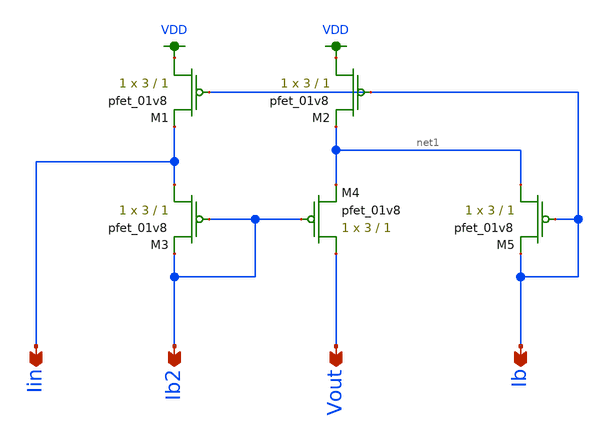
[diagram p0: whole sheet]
** sch_path: schematic/low-voltage_super-wilson.sch
**.subckt low-voltage_super-wilson Vout Ib Ib2 Iin
*.opin Vout
*.opin Ib
*.opin Ib2
*.opin Iin
XM1 VDD Ib Iin VDD sky130_fd_pr__pfet_01v8 L=1 W=3 nf=1 ad='int((nf+1)/2) * W/nf * 0.29' as='int((nf+2)/2) * W/nf * 0.29'
+ pd='2*int((nf+1)/2) * (W/nf + 0.29)' ps='2*int((nf+2)/2) * (W/nf + 0.29)' nrd='0.29 / W' nrs='0.29 / W'
+ sa=0 sb=0 sd=0 mult=1 m=1
XM2 VDD Ib net1 VDD sky130_fd_pr__pfet_01v8 L=1 W=3 nf=1 ad='int((nf+1)/2) * W/nf * 0.29' as='int((nf+2)/2) * W/nf * 0.29'
+ pd='2*int((nf+1)/2) * (W/nf + 0.29)' ps='2*int((nf+2)/2) * (W/nf + 0.29)' nrd='0.29 / W' nrs='0.29 / W'
+ sa=0 sb=0 sd=0 mult=1 m=1
XM3 Iin Ib2 Ib2 VDD sky130_fd_pr__pfet_01v8 L=1 W=3 nf=1 ad='int((nf+1)/2) * W/nf * 0.29' as='int((nf+2)/2) * W/nf * 0.29'
+ pd='2*int((nf+1)/2) * (W/nf + 0.29)' ps='2*int((nf+2)/2) * (W/nf + 0.29)' nrd='0.29 / W' nrs='0.29 / W'
+ sa=0 sb=0 sd=0 mult=1 m=1
XM4 Vout Ib2 net1 VDD sky130_fd_pr__pfet_01v8 L=1 W=3 nf=1 ad='int((nf+1)/2) * W/nf * 0.29' as='int((nf+2)/2) * W/nf * 0.29'
+ pd='2*int((nf+1)/2) * (W/nf + 0.29)' ps='2*int((nf+2)/2) * (W/nf + 0.29)' nrd='0.29 / W' nrs='0.29 / W'
+ sa=0 sb=0 sd=0 mult=1 m=1
XM5 net1 Ib Ib VDD sky130_fd_pr__pfet_01v8 L=1 W=3 nf=1 ad='int((nf+1)/2) * W/nf * 0.29' as='int((nf+2)/2) * W/nf * 0.29'
+ pd='2*int((nf+1)/2) * (W/nf + 0.29)' ps='2*int((nf+2)/2) * (W/nf + 0.29)' nrd='0.29 / W' nrs='0.29 / W'
+ sa=0 sb=0 sd=0 mult=1 m=1
**.ends
.GLOBAL VDD
.end
